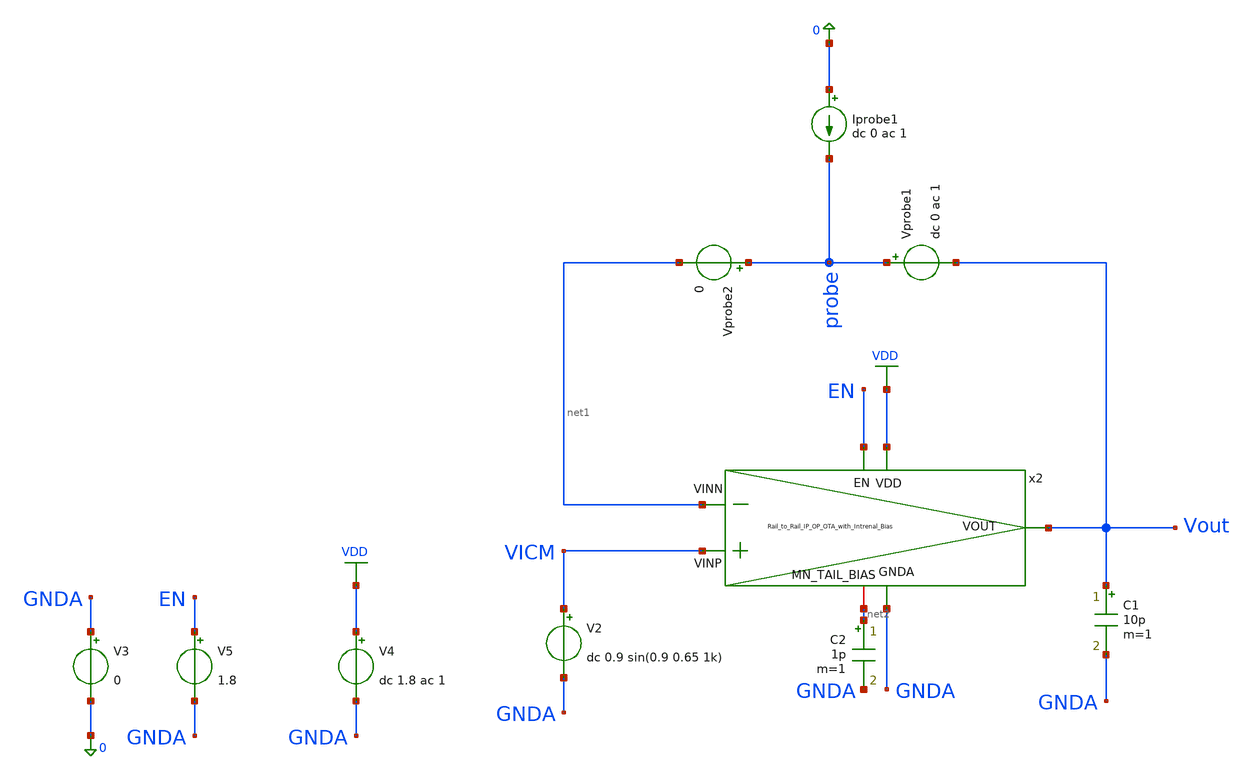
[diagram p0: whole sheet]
** sch_path: OTAs/Rail_to_Rail_OTA_Inp_IP/With_internal_Bias/tb_Rail_to_Rail_IP_OP_OTA_int_bias_STB.sch
.lib $::SKYWATER_MODELS/sky130.lib.spice tt
.include $::SKYWATER_STDCELLS/sky130_fd_sc_hd.spice

**.subckt tb_Rail_to_Rail_IP_OP_OTA_int_bias_STB
V3 GNDA 0 0
V5 EN GNDA 1.8
C1 Vout GNDA 10p m=1
Vprobe1 probe Vout dc 0 ac 1
Vprobe2 probe net1 0
Iprobe1 0 probe dc 0 ac 1
V2 VICM GNDA dc 0.9 sin(0.9 0.65 1k)
V4 VDD GNDA dc 1.8 ac 1
C2 net2 GNDA 1p m=1
x2 VDD EN net1 Vout VICM net2 GNDA Rail_to_Rail_IP_OP_OTA_with_Intrenal_Bias
**** begin user architecture code



.save @m.x1.xmn_bot_l2.msky130_fd_pr__nfet_01v8[gm]
.save @m.x1.xmn_bot_l2.msky130_fd_pr__nfet_01v8[gds]
.save @m.x1.xmn_bot_l2.msky130_fd_pr__nfet_01v8[vth]
.save @m.x1.xmn_bot_l2.msky130_fd_pr__nfet_01v8[vdsat]
.save @m.x1.xmn_bot_l2.msky130_fd_pr__nfet_01v8[cgg]
.save @m.x1.xmn_bot_l2.msky130_fd_pr__nfet_01v8[cgso]
.save @m.x1.xmn_bot_l2.msky130_fd_pr__nfet_01v8[cgdo]
.save @m.x1.xmn_casc_l2.msky130_fd_pr__nfet_01v8[gm]
.save @m.x1.xmn_casc_l2.msky130_fd_pr__nfet_01v8[gds]
.save @m.x1.xmn_casc_l2.msky130_fd_pr__nfet_01v8[vth]
.save @m.x1.xmn_casc_l2.msky130_fd_pr__nfet_01v8[vdsat]
.save @m.x1.xmn_casc_l2.msky130_fd_pr__nfet_01v8[cgg]
.save @m.x1.xmn_casc_l2.msky130_fd_pr__nfet_01v8[cgso]
.save @m.x1.xmn_casc_l2.msky130_fd_pr__nfet_01v8[cgdo]
.save @m.x1.xmn_bot_l1.msky130_fd_pr__nfet_01v8[gm]
.save @m.x1.xmn_bot_l1.msky130_fd_pr__nfet_01v8[gds]
.save @m.x1.xmn_bot_l1.msky130_fd_pr__nfet_01v8[vth]
.save @m.x1.xmn_bot_l1.msky130_fd_pr__nfet_01v8[vdsat]
.save @m.x1.xmn_bot_l1.msky130_fd_pr__nfet_01v8[cgg]
.save @m.x1.xmn_bot_l1.msky130_fd_pr__nfet_01v8[cgso]
.save @m.x1.xmn_bot_l1.msky130_fd_pr__nfet_01v8[cgdo]
.save @m.x1.xmn_casc_l1.msky130_fd_pr__nfet_01v8[gm]
.save @m.x1.xmn_casc_l1.msky130_fd_pr__nfet_01v8[gds]
.save @m.x1.xmn_casc_l1.msky130_fd_pr__nfet_01v8[vth]
.save @m.x1.xmn_casc_l1.msky130_fd_pr__nfet_01v8[vdsat]
.save @m.x1.xmn_casc_l1.msky130_fd_pr__nfet_01v8[cgg]
.save @m.x1.xmn_casc_l1.msky130_fd_pr__nfet_01v8[cgso]
.save @m.x1.xmn_casc_l1.msky130_fd_pr__nfet_01v8[cgdo]
.save @m.x1.xmp_casc_l2.msky130_fd_pr__pfet_01v8[gm]
.save @m.x1.xmp_casc_l2.msky130_fd_pr__pfet_01v8[gds]
.save @m.x1.xmp_casc_l2.msky130_fd_pr__pfet_01v8[vth]
.save @m.x1.xmp_casc_l2.msky130_fd_pr__pfet_01v8[vdsat]
.save @m.x1.xmp_casc_l2.msky130_fd_pr__pfet_01v8[cgg]
.save @m.x1.xmp_casc_l2.msky130_fd_pr__pfet_01v8[cgso]
.save @m.x1.xmp_casc_l2.msky130_fd_pr__pfet_01v8[cgdo]
.save @m.x1.xmp_casc_l1.msky130_fd_pr__pfet_01v8[gm]
.save @m.x1.xmp_casc_l1.msky130_fd_pr__pfet_01v8[gds]
.save @m.x1.xmp_casc_l1.msky130_fd_pr__pfet_01v8[vth]
.save @m.x1.xmp_casc_l1.msky130_fd_pr__pfet_01v8[vdsat]
.save @m.x1.xmp_casc_l1.msky130_fd_pr__pfet_01v8[cgg]
.save @m.x1.xmp_casc_l1.msky130_fd_pr__pfet_01v8[cgso]
.save @m.x1.xmp_casc_l1.msky130_fd_pr__pfet_01v8[cgdo]
.save @m.x1.xmp_top_l1.msky130_fd_pr__pfet_01v8[gm]
.save @m.x1.xmp_top_l1.msky130_fd_pr__pfet_01v8[gds]
.save @m.x1.xmp_top_l1.msky130_fd_pr__pfet_01v8[vth]
.save @m.x1.xmp_top_l1.msky130_fd_pr__pfet_01v8[vdsat]
.save @m.x1.xmp_top_l1.msky130_fd_pr__pfet_01v8[cgg]
.save @m.x1.xmp_top_l1.msky130_fd_pr__pfet_01v8[cgso]
.save @m.x1.xmp_top_l1.msky130_fd_pr__pfet_01v8[cgdo]
.save @m.x1.xmn_a1.msky130_fd_pr__nfet_01v8_lvt[gm]
.save @m.x1.xmn_a1.msky130_fd_pr__nfet_01v8_lvt[gds]
.save @m.x1.xmn_a1.msky130_fd_pr__nfet_01v8_lvt[vth]
.save @m.x1.xmn_a1.msky130_fd_pr__nfet_01v8_lvt[vdsat]
.save @m.x1.xmn_a1.msky130_fd_pr__nfet_01v8_lvt[cgg]
.save @m.x1.xmn_a1.msky130_fd_pr__nfet_01v8_lvt[cgso]
.save @m.x1.xmn_a1.msky130_fd_pr__nfet_01v8_lvt[cgdo]
.save @m.x1.xmn_a2.msky130_fd_pr__nfet_01v8_lvt[gm]
.save @m.x1.xmn_a2.msky130_fd_pr__nfet_01v8_lvt[gds]
.save @m.x1.xmn_a2.msky130_fd_pr__nfet_01v8_lvt[vth]
.save @m.x1.xmn_a2.msky130_fd_pr__nfet_01v8_lvt[vdsat]
.save @m.x1.xmn_a2.msky130_fd_pr__nfet_01v8_lvt[cgg]
.save @m.x1.xmn_a2.msky130_fd_pr__nfet_01v8_lvt[cgso]
.save @m.x1.xmn_a2.msky130_fd_pr__nfet_01v8_lvt[cgdo]
.save @m.x1.xmp_a1.msky130_fd_pr__pfet_01v8_lvt[gm]
.save @m.x1.xmp_a1.msky130_fd_pr__pfet_01v8_lvt[gds]
.save @m.x1.xmp_a1.msky130_fd_pr__pfet_01v8_lvt[vth]
.save @m.x1.xmp_a1.msky130_fd_pr__pfet_01v8_lvt[vdsat]
.save @m.x1.xmp_a1.msky130_fd_pr__pfet_01v8_lvt[cgg]
.save @m.x1.xmp_a1.msky130_fd_pr__pfet_01v8_lvt[cgso]
.save @m.x1.xmp_a1.msky130_fd_pr__pfet_01v8_lvt[cgdo]
.save @m.x1.xmp_a2.msky130_fd_pr__pfet_01v8_lvt[gm]
.save @m.x1.xmp_a2.msky130_fd_pr__pfet_01v8_lvt[gds]
.save @m.x1.xmp_a2.msky130_fd_pr__pfet_01v8_lvt[vth]
.save @m.x1.xmp_a2.msky130_fd_pr__pfet_01v8_lvt[vdsat]
.save @m.x1.xmp_a2.msky130_fd_pr__pfet_01v8_lvt[cgg]
.save @m.x1.xmp_a2.msky130_fd_pr__pfet_01v8_lvt[cgso]
.save @m.x1.xmp_a2.msky130_fd_pr__pfet_01v8_lvt[cgdo]
.save @m.x1.xmp_pdiff_bias.msky130_fd_pr__pfet_01v8[gm]
.save @m.x1.xmp_pdiff_bias.msky130_fd_pr__pfet_01v8[gds]
.save @m.x1.xmp_pdiff_bias.msky130_fd_pr__pfet_01v8[vth]
.save @m.x1.xmp_pdiff_bias.msky130_fd_pr__pfet_01v8[vdsat]
.save @m.x1.xmp_pdiff_bias.msky130_fd_pr__pfet_01v8[cgg]
.save @m.x1.xmp_pdiff_bias.msky130_fd_pr__pfet_01v8[cgso]
.save @m.x1.xmp_pdiff_bias.msky130_fd_pr__pfet_01v8[cgdo]
.save @m.x1.xmn_ndiff_bias.msky130_fd_pr__nfet_01v8[gm]
.save @m.x1.xmn_ndiff_bias.msky130_fd_pr__nfet_01v8[gds]
.save @m.x1.xmn_ndiff_bias.msky130_fd_pr__nfet_01v8[vth]
.save @m.x1.xmn_ndiff_bias.msky130_fd_pr__nfet_01v8[vdsat]
.save @m.x1.xmn_ndiff_bias.msky130_fd_pr__nfet_01v8[cgg]
.save @m.x1.xmn_ndiff_bias.msky130_fd_pr__nfet_01v8[cgso]
.save @m.x1.xmn_ndiff_bias.msky130_fd_pr__nfet_01v8[cgdo]
.save @m.x1.xmp_pdiff_bias_b.msky130_fd_pr__pfet_01v8[gm]
.save @m.x1.xmp_pdiff_bias_b.msky130_fd_pr__pfet_01v8[gds]
.save @m.x1.xmp_pdiff_bias_b.msky130_fd_pr__pfet_01v8[vth]
.save @m.x1.xmp_pdiff_bias_b.msky130_fd_pr__pfet_01v8[vdsat]
.save @m.x1.xmp_pdiff_bias_b.msky130_fd_pr__pfet_01v8[cgg]
.save @m.x1.xmp_pdiff_bias_b.msky130_fd_pr__pfet_01v8[cgso]
.save @m.x1.xmp_pdiff_bias_b.msky130_fd_pr__pfet_01v8[cgdo]
.save @m.x1.xmp_top_l2.msky130_fd_pr__pfet_01v8[gm]
.save @m.x1.xmp_top_l2.msky130_fd_pr__pfet_01v8[gds]
.save @m.x1.xmp_top_l2.msky130_fd_pr__pfet_01v8[vth]
.save @m.x1.xmp_top_l2.msky130_fd_pr__pfet_01v8[vdsat]
.save @m.x1.xmp_top_l2.msky130_fd_pr__pfet_01v8[cgg]
.save @m.x1.xmp_top_l2.msky130_fd_pr__pfet_01v8[cgso]
.save @m.x1.xmp_top_l2.msky130_fd_pr__pfet_01v8[cgdo]
.save @m.x1.xmn_bias_source.msky130_fd_pr__nfet_01v8[gm]
.save @m.x1.xmn_bias_source.msky130_fd_pr__nfet_01v8[gds]
.save @m.x1.xmn_bias_source.msky130_fd_pr__nfet_01v8[vth]
.save @m.x1.xmn_bias_source.msky130_fd_pr__nfet_01v8[vdsat]
.save @m.x1.xmn_bias_source.msky130_fd_pr__nfet_01v8[cgg]
.save @m.x1.xmn_bias_source.msky130_fd_pr__nfet_01v8[cgso]
.save @m.x1.xmn_bias_source.msky130_fd_pr__nfet_01v8[cgdo]
.save @m.x1.xmn_bias_ext.msky130_fd_pr__nfet_01v8[gm]
.save @m.x1.xmn_bias_ext.msky130_fd_pr__nfet_01v8[gds]
.save @m.x1.xmn_bias_ext.msky130_fd_pr__nfet_01v8[vth]
.save @m.x1.xmn_bias_ext.msky130_fd_pr__nfet_01v8[vdsat]
.save @m.x1.xmn_bias_ext.msky130_fd_pr__nfet_01v8[cgg]
.save @m.x1.xmn_bias_ext.msky130_fd_pr__nfet_01v8[cgso]
.save @m.x1.xmn_bias_ext.msky130_fd_pr__nfet_01v8[cgdo]
.save @m.x1.xmp_casc_b_source.msky130_fd_pr__pfet_01v8[gm]
.save @m.x1.xmp_casc_b_source.msky130_fd_pr__pfet_01v8[gds]
.save @m.x1.xmp_casc_b_source.msky130_fd_pr__pfet_01v8[vth]
.save @m.x1.xmp_casc_b_source.msky130_fd_pr__pfet_01v8[vdsat]
.save @m.x1.xmp_casc_b_source.msky130_fd_pr__pfet_01v8[cgg]
.save @m.x1.xmp_casc_b_source.msky130_fd_pr__pfet_01v8[cgso]
.save @m.x1.xmp_casc_b_source.msky130_fd_pr__pfet_01v8[cgdo]
.save @m.x1.xmn_casc_bias8.msky130_fd_pr__nfet_01v8[gm]
.save @m.x1.xmn_casc_bias8.msky130_fd_pr__nfet_01v8[gds]
.save @m.x1.xmn_casc_bias8.msky130_fd_pr__nfet_01v8[vth]
.save @m.x1.xmn_casc_bias8.msky130_fd_pr__nfet_01v8[vdsat]
.save @m.x1.xmn_casc_bias8.msky130_fd_pr__nfet_01v8[cgg]
.save @m.x1.xmn_casc_bias8.msky130_fd_pr__nfet_01v8[cgso]
.save @m.x1.xmn_casc_bias8.msky130_fd_pr__nfet_01v8[cgdo]
.save @m.x1.xmn_casc_b_source.msky130_fd_pr__nfet_01v8[gm]
.save @m.x1.xmn_casc_b_source.msky130_fd_pr__nfet_01v8[gds]
.save @m.x1.xmn_casc_b_source.msky130_fd_pr__nfet_01v8[vth]
.save @m.x1.xmn_casc_b_source.msky130_fd_pr__nfet_01v8[vdsat]
.save @m.x1.xmn_casc_b_source.msky130_fd_pr__nfet_01v8[cgg]
.save @m.x1.xmn_casc_b_source.msky130_fd_pr__nfet_01v8[cgso]
.save @m.x1.xmn_casc_b_source.msky130_fd_pr__nfet_01v8[cgdo]
.save @m.x1.xmp_casc_bias1.msky130_fd_pr__pfet_01v8[gm]
.save @m.x1.xmp_casc_bias1.msky130_fd_pr__pfet_01v8[gds]
.save @m.x1.xmp_casc_bias1.msky130_fd_pr__pfet_01v8[vth]
.save @m.x1.xmp_casc_bias1.msky130_fd_pr__pfet_01v8[vdsat]
.save @m.x1.xmp_casc_bias1.msky130_fd_pr__pfet_01v8[cgg]
.save @m.x1.xmp_casc_bias1.msky130_fd_pr__pfet_01v8[cgso]
.save @m.x1.xmp_casc_bias1.msky130_fd_pr__pfet_01v8[cgdo]
.save @m.x1.xmn_casc_bias7.msky130_fd_pr__nfet_01v8[gm]
.save @m.x1.xmn_casc_bias7.msky130_fd_pr__nfet_01v8[gds]
.save @m.x1.xmn_casc_bias7.msky130_fd_pr__nfet_01v8[vth]
.save @m.x1.xmn_casc_bias7.msky130_fd_pr__nfet_01v8[vdsat]
.save @m.x1.xmn_casc_bias7.msky130_fd_pr__nfet_01v8[cgg]
.save @m.x1.xmn_casc_bias7.msky130_fd_pr__nfet_01v8[cgso]
.save @m.x1.xmn_casc_bias7.msky130_fd_pr__nfet_01v8[cgdo]
.save @m.x1.xmn_casc_bias6.msky130_fd_pr__nfet_01v8[gm]
.save @m.x1.xmn_casc_bias6.msky130_fd_pr__nfet_01v8[gds]
.save @m.x1.xmn_casc_bias6.msky130_fd_pr__nfet_01v8[vth]
.save @m.x1.xmn_casc_bias6.msky130_fd_pr__nfet_01v8[vdsat]
.save @m.x1.xmn_casc_bias6.msky130_fd_pr__nfet_01v8[cgg]
.save @m.x1.xmn_casc_bias6.msky130_fd_pr__nfet_01v8[cgso]
.save @m.x1.xmn_casc_bias6.msky130_fd_pr__nfet_01v8[cgdo]
.save @m.x1.xmp_casc_bias2.msky130_fd_pr__pfet_01v8[gm]
.save @m.x1.xmp_casc_bias2.msky130_fd_pr__pfet_01v8[gds]
.save @m.x1.xmp_casc_bias2.msky130_fd_pr__pfet_01v8[vth]
.save @m.x1.xmp_casc_bias2.msky130_fd_pr__pfet_01v8[vdsat]
.save @m.x1.xmp_casc_bias2.msky130_fd_pr__pfet_01v8[cgg]
.save @m.x1.xmp_casc_bias2.msky130_fd_pr__pfet_01v8[cgso]
.save @m.x1.xmp_casc_bias2.msky130_fd_pr__pfet_01v8[cgdo]
.save @m.x1.xmp_casc_bias3.msky130_fd_pr__pfet_01v8[gm]
.save @m.x1.xmp_casc_bias3.msky130_fd_pr__pfet_01v8[gds]
.save @m.x1.xmp_casc_bias3.msky130_fd_pr__pfet_01v8[vth]
.save @m.x1.xmp_casc_bias3.msky130_fd_pr__pfet_01v8[vdsat]
.save @m.x1.xmp_casc_bias3.msky130_fd_pr__pfet_01v8[cgg]
.save @m.x1.xmp_casc_bias3.msky130_fd_pr__pfet_01v8[cgso]
.save @m.x1.xmp_casc_bias3.msky130_fd_pr__pfet_01v8[cgdo]
.save @m.x1.xmn_casc_bias5.msky130_fd_pr__nfet_01v8[gm]
.save @m.x1.xmn_casc_bias5.msky130_fd_pr__nfet_01v8[gds]
.save @m.x1.xmn_casc_bias5.msky130_fd_pr__nfet_01v8[vth]
.save @m.x1.xmn_casc_bias5.msky130_fd_pr__nfet_01v8[vdsat]
.save @m.x1.xmn_casc_bias5.msky130_fd_pr__nfet_01v8[cgg]
.save @m.x1.xmn_casc_bias5.msky130_fd_pr__nfet_01v8[cgso]
.save @m.x1.xmn_casc_bias5.msky130_fd_pr__nfet_01v8[cgdo]
.save @m.x1.xmn_casc_bias4.msky130_fd_pr__nfet_01v8[gm]
.save @m.x1.xmn_casc_bias4.msky130_fd_pr__nfet_01v8[gds]
.save @m.x1.xmn_casc_bias4.msky130_fd_pr__nfet_01v8[vth]
.save @m.x1.xmn_casc_bias4.msky130_fd_pr__nfet_01v8[vdsat]
.save @m.x1.xmn_casc_bias4.msky130_fd_pr__nfet_01v8[cgg]
.save @m.x1.xmn_casc_bias4.msky130_fd_pr__nfet_01v8[cgso]
.save @m.x1.xmn_casc_bias4.msky130_fd_pr__nfet_01v8[cgdo]
.save @m.x1.xmn_casc_bias3.msky130_fd_pr__nfet_01v8[gm]
.save @m.x1.xmn_casc_bias3.msky130_fd_pr__nfet_01v8[gds]
.save @m.x1.xmn_casc_bias3.msky130_fd_pr__nfet_01v8[vth]
.save @m.x1.xmn_casc_bias3.msky130_fd_pr__nfet_01v8[vdsat]
.save @m.x1.xmn_casc_bias3.msky130_fd_pr__nfet_01v8[cgg]
.save @m.x1.xmn_casc_bias3.msky130_fd_pr__nfet_01v8[cgso]
.save @m.x1.xmn_casc_bias3.msky130_fd_pr__nfet_01v8[cgdo]
.save @m.x1.xmn_casc_bias1.msky130_fd_pr__nfet_01v8[gm]
.save @m.x1.xmn_casc_bias1.msky130_fd_pr__nfet_01v8[gds]
.save @m.x1.xmn_casc_bias1.msky130_fd_pr__nfet_01v8[vth]
.save @m.x1.xmn_casc_bias1.msky130_fd_pr__nfet_01v8[vdsat]
.save @m.x1.xmn_casc_bias1.msky130_fd_pr__nfet_01v8[cgg]
.save @m.x1.xmn_casc_bias1.msky130_fd_pr__nfet_01v8[cgso]
.save @m.x1.xmn_casc_bias1.msky130_fd_pr__nfet_01v8[cgdo]
.save @m.x1.xmn_casc_bias2.msky130_fd_pr__nfet_01v8[gm]
.save @m.x1.xmn_casc_bias2.msky130_fd_pr__nfet_01v8[gds]
.save @m.x1.xmn_casc_bias2.msky130_fd_pr__nfet_01v8[vth]
.save @m.x1.xmn_casc_bias2.msky130_fd_pr__nfet_01v8[vdsat]
.save @m.x1.xmn_casc_bias2.msky130_fd_pr__nfet_01v8[cgg]
.save @m.x1.xmn_casc_bias2.msky130_fd_pr__nfet_01v8[cgso]
.save @m.x1.xmn_casc_bias2.msky130_fd_pr__nfet_01v8[cgdo]
.save @m.x1.xmn_sw1.msky130_fd_pr__nfet_01v8[gm]
.save @m.x1.xmn_sw1.msky130_fd_pr__nfet_01v8[gds]
.save @m.x1.xmn_sw1.msky130_fd_pr__nfet_01v8[vth]
.save @m.x1.xmn_sw1.msky130_fd_pr__nfet_01v8[vdsat]
.save @m.x1.xmn_sw1.msky130_fd_pr__nfet_01v8[cgg]
.save @m.x1.xmn_sw1.msky130_fd_pr__nfet_01v8[cgso]
.save @m.x1.xmn_sw1.msky130_fd_pr__nfet_01v8[cgdo]
.save @m.x1.xmp_sw1.msky130_fd_pr__pfet_01v8[gm]
.save @m.x1.xmp_sw1.msky130_fd_pr__pfet_01v8[gds]
.save @m.x1.xmp_sw1.msky130_fd_pr__pfet_01v8[vth]
.save @m.x1.xmp_sw1.msky130_fd_pr__pfet_01v8[vdsat]
.save @m.x1.xmp_sw1.msky130_fd_pr__pfet_01v8[cgg]
.save @m.x1.xmp_sw1.msky130_fd_pr__pfet_01v8[cgso]
.save @m.x1.xmp_sw1.msky130_fd_pr__pfet_01v8[cgdo]
.save @m.x1.xmp_sw2.msky130_fd_pr__pfet_01v8[gm]
.save @m.x1.xmp_sw2.msky130_fd_pr__pfet_01v8[gds]
.save @m.x1.xmp_sw2.msky130_fd_pr__pfet_01v8[vth]
.save @m.x1.xmp_sw2.msky130_fd_pr__pfet_01v8[vdsat]
.save @m.x1.xmp_sw2.msky130_fd_pr__pfet_01v8[cgg]
.save @m.x1.xmp_sw2.msky130_fd_pr__pfet_01v8[cgso]
.save @m.x1.xmp_sw2.msky130_fd_pr__pfet_01v8[cgdo]
.save @m.x1.xmn_sw2.msky130_fd_pr__nfet_01v8[gm]
.save @m.x1.xmn_sw2.msky130_fd_pr__nfet_01v8[gds]
.save @m.x1.xmn_sw2.msky130_fd_pr__nfet_01v8[vth]
.save @m.x1.xmn_sw2.msky130_fd_pr__nfet_01v8[vdsat]
.save @m.x1.xmn_sw2.msky130_fd_pr__nfet_01v8[cgg]
.save @m.x1.xmn_sw2.msky130_fd_pr__nfet_01v8[cgso]
.save @m.x1.xmn_sw2.msky130_fd_pr__nfet_01v8[cgdo]
.save @m.x1.xmp_sw3.msky130_fd_pr__pfet_01v8[gm]
.save @m.x1.xmp_sw3.msky130_fd_pr__pfet_01v8[gds]
.save @m.x1.xmp_sw3.msky130_fd_pr__pfet_01v8[vth]
.save @m.x1.xmp_sw3.msky130_fd_pr__pfet_01v8[vdsat]
.save @m.x1.xmp_sw3.msky130_fd_pr__pfet_01v8[cgg]
.save @m.x1.xmp_sw3.msky130_fd_pr__pfet_01v8[cgso]
.save @m.x1.xmp_sw3.msky130_fd_pr__pfet_01v8[cgdo]




.options savecurrents
.control
 save all
 let runs=2
 let run=0

 alter @Vprobe1[acmag]=1
 alter @iprobe1[acmag]=0

 dowhile run < runs
 set run =”$&run”
 ac dec 20 1 1e8
 write OTA_STB_TB_{$run}.raw
 all
 alter @Vprobe1[acmag]=0
 alter @iprobe1[acmag]=1
 let run = run + 1
 end

 let ip22 = ac2.i(Vprobe2)
 let vprb1 = ac1.probe
 let mb = 1/(vprb1+ip22)-1
 let phase_mb = 180/PI*vp(mb)
 plot vdb(mb)
 plot phase_mb
 plot vdb(mb) phase_mb
 echo -------------------------------
 echo -------------------------------
 meas ac peak MAX vmag(mb) FROM=2 TO=1.5GHZ
 let f3db = peak/sqrt(2)
 meas ac f1 WHEN vmag(mb)=f3db RISE=1
 meas ac BW WHEN vmag(mb)=f3db FALL=1
 let GBW = peak*BW
 meas ac pm_deg find phase_mb when vdb(mb)=0
 meas ac dominant_pole_f when vdb(mb)=0
 meas ac loop_gain find vdb(mb) at=0.01
 print GBW
 op
 **show m : gm : gmbs : gds : vds : vdsat : vgs : vth : id
.endc

**** end user architecture code
**.ends

* expanding   symbol:
*+  /home/nithin/eda/SKY130_DESIGN_IPS/OTAs/Rail_to_Rail_OTA_Inp_IP/Single_ended/With_internal_Bias/Rail_to_Rail_IP_OP_OTA_with_Intrenal_Bias.sym # of pins=7
** sym_path: OTAs/Rail_to_Rail_OTA_Inp_IP/With_internal_Bias/SCH/Rail_to_Rail_IP_OP_OTA_with_Intrenal_Bias.sym
** sch_path: OTAs/Rail_to_Rail_OTA_Inp_IP/With_internal_Bias/SCH/Rail_to_Rail_IP_OP_OTA_with_Intrenal_Bias.sch
.subckt Rail_to_Rail_IP_OP_OTA_with_Intrenal_Bias VDD EN VINN VOUT VINP MN_TAIL_BIAS GNDA
*.ipin VINP
*.ipin VINN
*.ipin VDD
*.ipin GNDA
*.opin VOUT
*.ipin EN
*.iopin MN_TAIL_BIAS
XMN_BOT_L2 net2 net8 GNDA GND sky130_fd_pr__nfet_01v8 L=2 W=0.5 nf=1 ad='int((1 + 1)/2) * 0.5 / 1 * 0.29'
+ as='int((1 + 2)/2) * 0.5 / 1 * 0.29' pd='2*int((1 + 1)/2) * (0.5 / 1 + 0.29)' ps='2*int((1 + 2)/2) * (0.5 / 1 + 0.29)'
+ nrd='0.29 / 0.5 ' nrs='0.29 / 0.5 ' sa=0 sb=0 sd=0 mult=6 m=6
XMN_CASC_L2 VOUT VBN_CASC net2 GND sky130_fd_pr__nfet_01v8 L=0.5 W=0.5 nf=1 ad='int((1 + 1)/2) * 0.5 / 1 * 0.29'
+ as='int((1 + 2)/2) * 0.5 / 1 * 0.29' pd='2*int((1 + 1)/2) * (0.5 / 1 + 0.29)' ps='2*int((1 + 2)/2) * (0.5 / 1 + 0.29)'
+ nrd='0.29 / 0.5 ' nrs='0.29 / 0.5 ' sa=0 sb=0 sd=0 mult=3 m=3
XMN_BOT_L1 net1 net8 GNDA GND sky130_fd_pr__nfet_01v8 L=2 W=0.5 nf=1 ad='int((1 + 1)/2) * 0.5 / 1 * 0.29'
+ as='int((1 + 2)/2) * 0.5 / 1 * 0.29' pd='2*int((1 + 1)/2) * (0.5 / 1 + 0.29)' ps='2*int((1 + 2)/2) * (0.5 / 1 + 0.29)'
+ nrd='0.29 / 0.5 ' nrs='0.29 / 0.5 ' sa=0 sb=0 sd=0 mult=6 m=6
XMN_CASC_L1 net5 VBN_CASC net1 GND sky130_fd_pr__nfet_01v8 L=0.5 W=0.5 nf=1 ad='int((1 + 1)/2) * 0.5 / 1 * 0.29'
+ as='int((1 + 2)/2) * 0.5 / 1 * 0.29' pd='2*int((1 + 1)/2) * (0.5 / 1 + 0.29)' ps='2*int((1 + 2)/2) * (0.5 / 1 + 0.29)'
+ nrd='0.29 / 0.5 ' nrs='0.29 / 0.5 ' sa=0 sb=0 sd=0 mult=3 m=3
XMP_CASC_L2 VOUT VBP_CASC net4 VDD sky130_fd_pr__pfet_01v8 L=0.5 W=0.5 nf=1 ad='int((1 + 1)/2) * 0.5 / 1 * 0.29'
+ as='int((1 + 2)/2) * 0.5 / 1 * 0.29' pd='2*int((1 + 1)/2) * (0.5 / 1 + 0.29)' ps='2*int((1 + 2)/2) * (0.5 / 1 + 0.29)'
+ nrd='0.29 / 0.5 ' nrs='0.29 / 0.5 ' sa=0 sb=0 sd=0 mult=8 m=8
XMP_CASC_L1 net5 VBP_CASC net3 VDD sky130_fd_pr__pfet_01v8 L=0.5 W=0.5 nf=1 ad='int((1 + 1)/2) * 0.5 / 1 * 0.29'
+ as='int((1 + 2)/2) * 0.5 / 1 * 0.29' pd='2*int((1 + 1)/2) * (0.5 / 1 + 0.29)' ps='2*int((1 + 2)/2) * (0.5 / 1 + 0.29)'
+ nrd='0.29 / 0.5 ' nrs='0.29 / 0.5 ' sa=0 sb=0 sd=0 mult=8 m=8
XMP_TOP_L1 net3 net5 VDD VDD sky130_fd_pr__pfet_01v8 L=2 W=2 nf=1 ad='int((1 + 1)/2) * 2 / 1 * 0.29'
+ as='int((1 + 2)/2) * 2 / 1 * 0.29' pd='2*int((1 + 1)/2) * (2 / 1 + 0.29)' ps='2*int((1 + 2)/2) * (2 / 1 + 0.29)'
+ nrd='0.29 / 2 ' nrs='0.29 / 2 ' sa=0 sb=0 sd=0 mult=6 m=6
XMN_A1 net3 VINP net6 GND sky130_fd_pr__nfet_01v8_lvt L=2 W=2.5 nf=1 ad='int((1 + 1)/2) * 2.5 / 1 * 0.29'
+ as='int((1 + 2)/2) * 2.5 / 1 * 0.29' pd='2*int((1 + 1)/2) * (2.5 / 1 + 0.29)' ps='2*int((1 + 2)/2) * (2.5 / 1 + 0.29)'
+ nrd='0.29 / 2.5 ' nrs='0.29 / 2.5 ' sa=0 sb=0 sd=0 mult=8 m=8
XMN_A2 net4 VINN net6 GND sky130_fd_pr__nfet_01v8_lvt L=2 W=2.5 nf=1 ad='int((1 + 1)/2) * 2.5 / 1 * 0.29'
+ as='int((1 + 2)/2) * 2.5 / 1 * 0.29' pd='2*int((1 + 1)/2) * (2.5 / 1 + 0.29)' ps='2*int((1 + 2)/2) * (2.5 / 1 + 0.29)'
+ nrd='0.29 / 2.5 ' nrs='0.29 / 2.5 ' sa=0 sb=0 sd=0 mult=8 m=8
XMP_A1 net1 VINP net7 VDD sky130_fd_pr__pfet_01v8_lvt L=2 W=4 nf=1 ad='int((1 + 1)/2) * 4 / 1 * 0.29'
+ as='int((1 + 2)/2) * 4 / 1 * 0.29' pd='2*int((1 + 1)/2) * (4 / 1 + 0.29)' ps='2*int((1 + 2)/2) * (4 / 1 + 0.29)'
+ nrd='0.29 / 4 ' nrs='0.29 / 4 ' sa=0 sb=0 sd=0 mult=28 m=28
XMP_A2 net2 VINN net7 VDD sky130_fd_pr__pfet_01v8_lvt L=2 W=4 nf=1 ad='int((1 + 1)/2) * 4 / 1 * 0.29'
+ as='int((1 + 2)/2) * 4 / 1 * 0.29' pd='2*int((1 + 1)/2) * (4 / 1 + 0.29)' ps='2*int((1 + 2)/2) * (4 / 1 + 0.29)'
+ nrd='0.29 / 4 ' nrs='0.29 / 4 ' sa=0 sb=0 sd=0 mult=28 m=28
XMP_PDIFF_BIAS net7 net9 VDD VDD sky130_fd_pr__pfet_01v8 L=2 W=2 nf=1 ad='int((1 + 1)/2) * 2 / 1 * 0.29'
+ as='int((1 + 2)/2) * 2 / 1 * 0.29' pd='2*int((1 + 1)/2) * (2 / 1 + 0.29)' ps='2*int((1 + 2)/2) * (2 / 1 + 0.29)'
+ nrd='0.29 / 2 ' nrs='0.29 / 2 ' sa=0 sb=0 sd=0 mult=8 m=8
XMN_NDIFF_BIAS net6 net8 GNDA GND sky130_fd_pr__nfet_01v8 L=2 W=0.5 nf=1 ad='int((1 + 1)/2) * 0.5 / 1 * 0.29'
+ as='int((1 + 2)/2) * 0.5 / 1 * 0.29' pd='2*int((1 + 1)/2) * (0.5 / 1 + 0.29)' ps='2*int((1 + 2)/2) * (0.5 / 1 + 0.29)'
+ nrd='0.29 / 0.5 ' nrs='0.29 / 0.5 ' sa=0 sb=0 sd=0 mult=8 m=8
XMP_PDIFF_BIAS_B net9 net9 VDD VDD sky130_fd_pr__pfet_01v8 L=2 W=2 nf=1 ad='int((1 + 1)/2) * 2 / 1 * 0.29'
+ as='int((1 + 2)/2) * 2 / 1 * 0.29' pd='2*int((1 + 1)/2) * (2 / 1 + 0.29)' ps='2*int((1 + 2)/2) * (2 / 1 + 0.29)'
+ nrd='0.29 / 2 ' nrs='0.29 / 2 ' sa=0 sb=0 sd=0 mult=1 m=1
XMP_TOP_L2 net4 net5 VDD VDD sky130_fd_pr__pfet_01v8 L=2 W=2 nf=1 ad='int((1 + 1)/2) * 2 / 1 * 0.29'
+ as='int((1 + 2)/2) * 2 / 1 * 0.29' pd='2*int((1 + 1)/2) * (2 / 1 + 0.29)' ps='2*int((1 + 2)/2) * (2 / 1 + 0.29)'
+ nrd='0.29 / 2 ' nrs='0.29 / 2 ' sa=0 sb=0 sd=0 mult=6 m=6
XMN_BIAS_SOURCE net9 net8 GNDA GND sky130_fd_pr__nfet_01v8 L=2 W=0.5 nf=1 ad='int((1 + 1)/2) * 0.5 / 1 * 0.29'
+ as='int((1 + 2)/2) * 0.5 / 1 * 0.29' pd='2*int((1 + 1)/2) * (0.5 / 1 + 0.29)' ps='2*int((1 + 2)/2) * (0.5 / 1 + 0.29)'
+ nrd='0.29 / 0.5 ' nrs='0.29 / 0.5 ' sa=0 sb=0 sd=0 mult=1 m=1
XMN_BIAS_EXT net8 net8 GNDA GND sky130_fd_pr__nfet_01v8 L=2 W=0.5 nf=1 ad='int((1 + 1)/2) * 0.5 / 1 * 0.29'
+ as='int((1 + 2)/2) * 0.5 / 1 * 0.29' pd='2*int((1 + 1)/2) * (0.5 / 1 + 0.29)' ps='2*int((1 + 2)/2) * (0.5 / 1 + 0.29)'
+ nrd='0.29 / 0.5 ' nrs='0.29 / 0.5 ' sa=0 sb=0 sd=0 mult=1 m=1
XMP_CASC_B_SOURCE VBN_CASC net9 VDD VDD sky130_fd_pr__pfet_01v8 L=2 W=2 nf=1 ad='int((1 + 1)/2) * 2 / 1 * 0.29'
+ as='int((1 + 2)/2) * 2 / 1 * 0.29' pd='2*int((1 + 1)/2) * (2 / 1 + 0.29)' ps='2*int((1 + 2)/2) * (2 / 1 + 0.29)'
+ nrd='0.29 / 2 ' nrs='0.29 / 2 ' sa=0 sb=0 sd=0 mult=1 m=1
XMN_CASC_BIAS8 net16 VBN_CASC GNDA GND sky130_fd_pr__nfet_01v8 L=0.5 W=0.5 nf=1 ad='int((1 + 1)/2) * 0.5 / 1 * 0.29'
+ as='int((1 + 2)/2) * 0.5 / 1 * 0.29' pd='2*int((1 + 1)/2) * (0.5 / 1 + 0.29)' ps='2*int((1 + 2)/2) * (0.5 / 1 + 0.29)'
+ nrd='0.29 / 0.5 ' nrs='0.29 / 0.5 ' sa=0 sb=0 sd=0 mult=1 m=1
XMN_CASC_B_SOURCE VBP_CASC net8 GNDA GND sky130_fd_pr__nfet_01v8 L=2 W=0.5 nf=1 ad='int((1 + 1)/2) * 0.5 / 1 * 0.29'
+ as='int((1 + 2)/2) * 0.5 / 1 * 0.29' pd='2*int((1 + 1)/2) * (0.5 / 1 + 0.29)' ps='2*int((1 + 2)/2) * (0.5 / 1 + 0.29)'
+ nrd='0.29 / 0.5 ' nrs='0.29 / 0.5 ' sa=0 sb=0 sd=0 mult=1 m=1
XMP_CASC_BIAS1 net11 VBP_CASC VDD VDD sky130_fd_pr__pfet_01v8 L=0.5 W=0.5 nf=1 ad='int((1 + 1)/2) * 0.5 / 1 * 0.29'
+ as='int((1 + 2)/2) * 0.5 / 1 * 0.29' pd='2*int((1 + 1)/2) * (0.5 / 1 + 0.29)' ps='2*int((1 + 2)/2) * (0.5 / 1 + 0.29)'
+ nrd='0.29 / 0.5 ' nrs='0.29 / 0.5 ' sa=0 sb=0 sd=0 mult=1 m=1
XMN_CASC_BIAS7 net17 VBN_CASC net16 GND sky130_fd_pr__nfet_01v8 L=0.5 W=0.5 nf=1 ad='int((1 + 1)/2) * 0.5 / 1 * 0.29'
+ as='int((1 + 2)/2) * 0.5 / 1 * 0.29' pd='2*int((1 + 1)/2) * (0.5 / 1 + 0.29)' ps='2*int((1 + 2)/2) * (0.5 / 1 + 0.29)'
+ nrd='0.29 / 0.5 ' nrs='0.29 / 0.5 ' sa=0 sb=0 sd=0 mult=1 m=1
XMN_CASC_BIAS6 net18 VBN_CASC net17 GND sky130_fd_pr__nfet_01v8 L=0.5 W=0.5 nf=1 ad='int((1 + 1)/2) * 0.5 / 1 * 0.29'
+ as='int((1 + 2)/2) * 0.5 / 1 * 0.29' pd='2*int((1 + 1)/2) * (0.5 / 1 + 0.29)' ps='2*int((1 + 2)/2) * (0.5 / 1 + 0.29)'
+ nrd='0.29 / 0.5 ' nrs='0.29 / 0.5 ' sa=0 sb=0 sd=0 mult=1 m=1
XMP_CASC_BIAS2 net10 VBP_CASC net11 VDD sky130_fd_pr__pfet_01v8 L=0.5 W=0.5 nf=1 ad='int((1 + 1)/2) * 0.5 / 1 * 0.29'
+ as='int((1 + 2)/2) * 0.5 / 1 * 0.29' pd='2*int((1 + 1)/2) * (0.5 / 1 + 0.29)' ps='2*int((1 + 2)/2) * (0.5 / 1 + 0.29)'
+ nrd='0.29 / 0.5 ' nrs='0.29 / 0.5 ' sa=0 sb=0 sd=0 mult=1 m=1
XMP_CASC_BIAS3 VBP_CASC VBP_CASC net10 VDD sky130_fd_pr__pfet_01v8 L=0.5 W=0.5 nf=1 ad='int((1 + 1)/2) * 0.5 / 1 * 0.29'
+ as='int((1 + 2)/2) * 0.5 / 1 * 0.29' pd='2*int((1 + 1)/2) * (0.5 / 1 + 0.29)' ps='2*int((1 + 2)/2) * (0.5 / 1 + 0.29)'
+ nrd='0.29 / 0.5 ' nrs='0.29 / 0.5 ' sa=0 sb=0 sd=0 mult=1 m=1
XMN_CASC_BIAS5 net19 VBN_CASC net18 GND sky130_fd_pr__nfet_01v8 L=0.5 W=0.5 nf=1 ad='int((1 + 1)/2) * 0.5 / 1 * 0.29'
+ as='int((1 + 2)/2) * 0.5 / 1 * 0.29' pd='2*int((1 + 1)/2) * (0.5 / 1 + 0.29)' ps='2*int((1 + 2)/2) * (0.5 / 1 + 0.29)'
+ nrd='0.29 / 0.5 ' nrs='0.29 / 0.5 ' sa=0 sb=0 sd=0 mult=1 m=1
XMN_CASC_BIAS4 net20 VBN_CASC net19 GND sky130_fd_pr__nfet_01v8 L=0.5 W=0.5 nf=1 ad='int((1 + 1)/2) * 0.5 / 1 * 0.29'
+ as='int((1 + 2)/2) * 0.5 / 1 * 0.29' pd='2*int((1 + 1)/2) * (0.5 / 1 + 0.29)' ps='2*int((1 + 2)/2) * (0.5 / 1 + 0.29)'
+ nrd='0.29 / 0.5 ' nrs='0.29 / 0.5 ' sa=0 sb=0 sd=0 mult=1 m=1
XMN_CASC_BIAS3 net21 VBN_CASC net20 GND sky130_fd_pr__nfet_01v8 L=0.5 W=0.5 nf=1 ad='int((1 + 1)/2) * 0.5 / 1 * 0.29'
+ as='int((1 + 2)/2) * 0.5 / 1 * 0.29' pd='2*int((1 + 1)/2) * (0.5 / 1 + 0.29)' ps='2*int((1 + 2)/2) * (0.5 / 1 + 0.29)'
+ nrd='0.29 / 0.5 ' nrs='0.29 / 0.5 ' sa=0 sb=0 sd=0 mult=1 m=1
XMN_CASC_BIAS1 VBN_CASC VBN_CASC net22 GND sky130_fd_pr__nfet_01v8 L=0.5 W=0.5 nf=1 ad='int((1 + 1)/2) * 0.5 / 1 * 0.29'
+ as='int((1 + 2)/2) * 0.5 / 1 * 0.29' pd='2*int((1 + 1)/2) * (0.5 / 1 + 0.29)' ps='2*int((1 + 2)/2) * (0.5 / 1 + 0.29)'
+ nrd='0.29 / 0.5 ' nrs='0.29 / 0.5 ' sa=0 sb=0 sd=0 mult=1 m=1
XMN_CASC_BIAS2 net22 VBN_CASC net21 GND sky130_fd_pr__nfet_01v8 L=0.5 W=0.5 nf=1 ad='int((1 + 1)/2) * 0.5 / 1 * 0.29'
+ as='int((1 + 2)/2) * 0.5 / 1 * 0.29' pd='2*int((1 + 1)/2) * (0.5 / 1 + 0.29)' ps='2*int((1 + 2)/2) * (0.5 / 1 + 0.29)'
+ nrd='0.29 / 0.5 ' nrs='0.29 / 0.5 ' sa=0 sb=0 sd=0 mult=1 m=1
XMN_SW1 net8 EN_B GNDA GND sky130_fd_pr__nfet_01v8 L=1 W=1 nf=1 ad='int((1 + 1)/2) * 1 / 1 * 0.29' as='int((1 + 2)/2) * 1 / 1 * 0.29'
+ pd='2*int((1 + 1)/2) * (1 / 1 + 0.29)' ps='2*int((1 + 2)/2) * (1 / 1 + 0.29)' nrd='0.29 / 1 ' nrs='0.29 / 1 '
+ sa=0 sb=0 sd=0 mult=1 m=1
XMP_SW1 net9 EN VDD VDD sky130_fd_pr__pfet_01v8 L=2 W=2 nf=1 ad='int((1 + 1)/2) * 2 / 1 * 0.29' as='int((1 + 2)/2) * 2 / 1 * 0.29'
+ pd='2*int((1 + 1)/2) * (2 / 1 + 0.29)' ps='2*int((1 + 2)/2) * (2 / 1 + 0.29)' nrd='0.29 / 2 ' nrs='0.29 / 2 '
+ sa=0 sb=0 sd=0 mult=1 m=1
XMP_SW2 VBP_CASC EN VDD VDD sky130_fd_pr__pfet_01v8 L=2 W=2 nf=1 ad='int((1 + 1)/2) * 2 / 1 * 0.29' as='int((1 + 2)/2) * 2 / 1 * 0.29'
+ pd='2*int((1 + 1)/2) * (2 / 1 + 0.29)' ps='2*int((1 + 2)/2) * (2 / 1 + 0.29)' nrd='0.29 / 2 ' nrs='0.29 / 2 '
+ sa=0 sb=0 sd=0 mult=1 m=1
XMN_SW2 VBN_CASC EN_B GNDA GND sky130_fd_pr__nfet_01v8 L=2 W=1 nf=1 ad='int((1 + 1)/2) * 1 / 1 * 0.29'
+ as='int((1 + 2)/2) * 1 / 1 * 0.29' pd='2*int((1 + 1)/2) * (1 / 1 + 0.29)' ps='2*int((1 + 2)/2) * (1 / 1 + 0.29)'
+ nrd='0.29 / 1 ' nrs='0.29 / 1 ' sa=0 sb=0 sd=0 mult=1 m=1
XMP_SW3 net5 EN VDD VDD sky130_fd_pr__pfet_01v8 L=2 W=2 nf=1 ad='int((1 + 1)/2) * 2 / 1 * 0.29' as='int((1 + 2)/2) * 2 / 1 * 0.29'
+ pd='2*int((1 + 1)/2) * (2 / 1 + 0.29)' ps='2*int((1 + 2)/2) * (2 / 1 + 0.29)' nrd='0.29 / 2 ' nrs='0.29 / 2 '
+ sa=0 sb=0 sd=0 mult=1 m=1
.save v(vdd)
.save v(net7)
XM1 VBP_TOP MN_TAIL_BIAS net12 GND sky130_fd_pr__nfet_01v8 L=4 W=10 nf=1 ad='int((1 + 1)/2) * 10 / 1 * 0.29'
+ as='int((1 + 2)/2) * 10 / 1 * 0.29' pd='2*int((1 + 1)/2) * (10 / 1 + 0.29)' ps='2*int((1 + 2)/2) * (10 / 1 + 0.29)'
+ nrd='0.29 / 10 ' nrs='0.29 / 10 ' sa=0 sb=0 sd=0 mult=16 m=16
XM3 VBP_TOP VBP_TOP VDD VDD sky130_fd_pr__pfet_01v8 L=2 W=2 nf=1 ad='int((1 + 1)/2) * 2 / 1 * 0.29' as='int((1 + 2)/2) * 2 / 1 * 0.29'
+ pd='2*int((1 + 1)/2) * (2 / 1 + 0.29)' ps='2*int((1 + 2)/2) * (2 / 1 + 0.29)' nrd='0.29 / 2 ' nrs='0.29 / 2 '
+ sa=0 sb=0 sd=0 mult=1 m=1
XM4 MN_TAIL_BIAS VBP_TOP VDD VDD sky130_fd_pr__pfet_01v8 L=2 W=2 nf=1 ad='int((1 + 1)/2) * 2 / 1 * 0.29'
+ as='int((1 + 2)/2) * 2 / 1 * 0.29' pd='2*int((1 + 1)/2) * (2 / 1 + 0.29)' ps='2*int((1 + 2)/2) * (2 / 1 + 0.29)'
+ nrd='0.29 / 2 ' nrs='0.29 / 2 ' sa=0 sb=0 sd=0 mult=1 m=1
XM10 MN_TAIL_BIAS MN_TAIL_BIAS GNDA GND sky130_fd_pr__nfet_01v8 L=4 W=10 nf=1 ad='int((1 + 1)/2) * 10 / 1 * 0.29'
+ as='int((1 + 2)/2) * 10 / 1 * 0.29' pd='2*int((1 + 1)/2) * (10 / 1 + 0.29)' ps='2*int((1 + 2)/2) * (10 / 1 + 0.29)'
+ nrd='0.29 / 10 ' nrs='0.29 / 10 ' sa=0 sb=0 sd=0 mult=4 m=4
XM16 MN_TAIL_BIAS EN_B GNDA GND sky130_fd_pr__nfet_01v8 L=6.4 W=0.5 nf=1 ad='int((1 + 1)/2) * 0.5 / 1 * 0.29'
+ as='int((1 + 2)/2) * 0.5 / 1 * 0.29' pd='2*int((1 + 1)/2) * (0.5 / 1 + 0.29)' ps='2*int((1 + 2)/2) * (0.5 / 1 + 0.29)'
+ nrd='0.29 / 0.5 ' nrs='0.29 / 0.5 ' sa=0 sb=0 sd=0 mult=1 m=1
XR14 net23 net12 GNDA sky130_fd_pr__res_xhigh_po_1p41 L=6.4 mult=1 m=1
XR15 net24 net23 GNDA sky130_fd_pr__res_xhigh_po_1p41 L=6.4 mult=1 m=1
XR16 net25 net24 GNDA sky130_fd_pr__res_xhigh_po_1p41 L=6.4 mult=1 m=1
XR17 net26 net25 GNDA sky130_fd_pr__res_xhigh_po_1p41 L=6.4 mult=1 m=1
XR18 net27 net26 GNDA sky130_fd_pr__res_xhigh_po_1p41 L=6.4 mult=1 m=1
XR19 net28 net27 GNDA sky130_fd_pr__res_xhigh_po_1p41 L=6.4 mult=1 m=1
XR20 net29 net28 GNDA sky130_fd_pr__res_xhigh_po_1p41 L=6.4 mult=1 m=1
XR21 net30 net29 GNDA sky130_fd_pr__res_xhigh_po_1p41 L=6.4 mult=1 m=1
XR22 GNDA net30 GNDA sky130_fd_pr__res_xhigh_po_1p41 L=6.4 mult=1 m=1
XM15 VBP_TOP EN VDD VDD sky130_fd_pr__pfet_01v8 L=1 W=0.5 nf=1 ad='int((1 + 1)/2) * 0.5 / 1 * 0.29' as='int((1 + 2)/2) * 0.5 / 1 * 0.29'
+ pd='2*int((1 + 1)/2) * (0.5 / 1 + 0.29)' ps='2*int((1 + 2)/2) * (0.5 / 1 + 0.29)' nrd='0.29 / 0.5 ' nrs='0.29 / 0.5 '
+ sa=0 sb=0 sd=0 mult=1 m=1
XM2 VSTRP_IP VBP_TOP VDD VDD sky130_fd_pr__pfet_01v8 L=2 W=2 nf=1 ad='int((1 + 1)/2) * 2 / 1 * 0.29'
+ as='int((1 + 2)/2) * 2 / 1 * 0.29' pd='2*int((1 + 1)/2) * (2 / 1 + 0.29)' ps='2*int((1 + 2)/2) * (2 / 1 + 0.29)'
+ nrd='0.29 / 2 ' nrs='0.29 / 2 ' sa=0 sb=0 sd=0 mult=7 m=7
XM19 VSTRP_IP VDD net31 GNDA sky130_fd_pr__nfet_01v8 L=10 W=0.5 nf=1 ad='int((1 + 1)/2) * 0.5 / 1 * 0.29'
+ as='int((1 + 2)/2) * 0.5 / 1 * 0.29' pd='2*int((1 + 1)/2) * (0.5 / 1 + 0.29)' ps='2*int((1 + 2)/2) * (0.5 / 1 + 0.29)'
+ nrd='0.29 / 0.5 ' nrs='0.29 / 0.5 ' sa=0 sb=0 sd=0 mult=1 m=1
XM20 net31 VDD net32 GNDA sky130_fd_pr__nfet_01v8 L=10 W=0.5 nf=1 ad='int((1 + 1)/2) * 0.5 / 1 * 0.29'
+ as='int((1 + 2)/2) * 0.5 / 1 * 0.29' pd='2*int((1 + 1)/2) * (0.5 / 1 + 0.29)' ps='2*int((1 + 2)/2) * (0.5 / 1 + 0.29)'
+ nrd='0.29 / 0.5 ' nrs='0.29 / 0.5 ' sa=0 sb=0 sd=0 mult=1 m=1
XM21 net32 VDD net33 GNDA sky130_fd_pr__nfet_01v8 L=10 W=0.5 nf=1 ad='int((1 + 1)/2) * 0.5 / 1 * 0.29'
+ as='int((1 + 2)/2) * 0.5 / 1 * 0.29' pd='2*int((1 + 1)/2) * (0.5 / 1 + 0.29)' ps='2*int((1 + 2)/2) * (0.5 / 1 + 0.29)'
+ nrd='0.29 / 0.5 ' nrs='0.29 / 0.5 ' sa=0 sb=0 sd=0 mult=1 m=1
XM26 net33 VDD net34 GNDA sky130_fd_pr__nfet_01v8 L=10 W=0.5 nf=1 ad='int((1 + 1)/2) * 0.5 / 1 * 0.29'
+ as='int((1 + 2)/2) * 0.5 / 1 * 0.29' pd='2*int((1 + 1)/2) * (0.5 / 1 + 0.29)' ps='2*int((1 + 2)/2) * (0.5 / 1 + 0.29)'
+ nrd='0.29 / 0.5 ' nrs='0.29 / 0.5 ' sa=0 sb=0 sd=0 mult=1 m=1
XM27 net34 VDD net35 GNDA sky130_fd_pr__nfet_01v8 L=10 W=0.5 nf=1 ad='int((1 + 1)/2) * 0.5 / 1 * 0.29'
+ as='int((1 + 2)/2) * 0.5 / 1 * 0.29' pd='2*int((1 + 1)/2) * (0.5 / 1 + 0.29)' ps='2*int((1 + 2)/2) * (0.5 / 1 + 0.29)'
+ nrd='0.29 / 0.5 ' nrs='0.29 / 0.5 ' sa=0 sb=0 sd=0 mult=1 m=1
XM28 net35 VDD net36 GNDA sky130_fd_pr__nfet_01v8 L=10 W=0.5 nf=1 ad='int((1 + 1)/2) * 0.5 / 1 * 0.29'
+ as='int((1 + 2)/2) * 0.5 / 1 * 0.29' pd='2*int((1 + 1)/2) * (0.5 / 1 + 0.29)' ps='2*int((1 + 2)/2) * (0.5 / 1 + 0.29)'
+ nrd='0.29 / 0.5 ' nrs='0.29 / 0.5 ' sa=0 sb=0 sd=0 mult=1 m=1
XM29 net36 VDD net37 GNDA sky130_fd_pr__nfet_01v8 L=10 W=0.5 nf=1 ad='int((1 + 1)/2) * 0.5 / 1 * 0.29'
+ as='int((1 + 2)/2) * 0.5 / 1 * 0.29' pd='2*int((1 + 1)/2) * (0.5 / 1 + 0.29)' ps='2*int((1 + 2)/2) * (0.5 / 1 + 0.29)'
+ nrd='0.29 / 0.5 ' nrs='0.29 / 0.5 ' sa=0 sb=0 sd=0 mult=1 m=1
XM30 net37 VDD net38 GNDA sky130_fd_pr__nfet_01v8 L=10 W=0.5 nf=1 ad='int((1 + 1)/2) * 0.5 / 1 * 0.29'
+ as='int((1 + 2)/2) * 0.5 / 1 * 0.29' pd='2*int((1 + 1)/2) * (0.5 / 1 + 0.29)' ps='2*int((1 + 2)/2) * (0.5 / 1 + 0.29)'
+ nrd='0.29 / 0.5 ' nrs='0.29 / 0.5 ' sa=0 sb=0 sd=0 mult=1 m=1
XM31 net38 VDD net39 GNDA sky130_fd_pr__nfet_01v8 L=10 W=0.5 nf=1 ad='int((1 + 1)/2) * 0.5 / 1 * 0.29'
+ as='int((1 + 2)/2) * 0.5 / 1 * 0.29' pd='2*int((1 + 1)/2) * (0.5 / 1 + 0.29)' ps='2*int((1 + 2)/2) * (0.5 / 1 + 0.29)'
+ nrd='0.29 / 0.5 ' nrs='0.29 / 0.5 ' sa=0 sb=0 sd=0 mult=1 m=1
XM32 net39 VDD GNDA GNDA sky130_fd_pr__nfet_01v8 L=10 W=0.5 nf=1 ad='int((1 + 1)/2) * 0.5 / 1 * 0.29'
+ as='int((1 + 2)/2) * 0.5 / 1 * 0.29' pd='2*int((1 + 1)/2) * (0.5 / 1 + 0.29)' ps='2*int((1 + 2)/2) * (0.5 / 1 + 0.29)'
+ nrd='0.29 / 0.5 ' nrs='0.29 / 0.5 ' sa=0 sb=0 sd=0 mult=1 m=1
XM12 MN_TAIL_BIAS VSTRP_OUT net15 VDD sky130_fd_pr__pfet_01v8 L=4 W=0.5 nf=1 ad='int((1 + 1)/2) * 0.5 / 1 * 0.29'
+ as='int((1 + 2)/2) * 0.5 / 1 * 0.29' pd='2*int((1 + 1)/2) * (0.5 / 1 + 0.29)' ps='2*int((1 + 2)/2) * (0.5 / 1 + 0.29)'
+ nrd='0.29 / 0.5 ' nrs='0.29 / 0.5 ' sa=0 sb=0 sd=0 mult=1 m=1
XR24 net40 VDD GNDA sky130_fd_pr__res_xhigh_po_1p41 L=7.05 mult=1 m=1
XR25 net41 net40 GNDA sky130_fd_pr__res_xhigh_po_1p41 L=7.05 mult=1 m=1
XR26 net42 net41 GNDA sky130_fd_pr__res_xhigh_po_1p41 L=7.05 mult=1 m=1
XR27 net43 net42 GNDA sky130_fd_pr__res_xhigh_po_1p41 L=7.05 mult=1 m=1
XR28 net44 net43 GNDA sky130_fd_pr__res_xhigh_po_1p41 L=7.05 mult=1 m=1
XR29 net45 net44 GNDA sky130_fd_pr__res_xhigh_po_1p41 L=7.05 mult=1 m=1
XR30 net46 net45 GNDA sky130_fd_pr__res_xhigh_po_1p41 L=7.05 mult=1 m=1
XR31 net47 net46 GNDA sky130_fd_pr__res_xhigh_po_1p41 L=7.05 mult=1 m=1
XR34 net15 net47 GNDA sky130_fd_pr__res_xhigh_po_1p41 L=7.05 mult=1 m=1
XM5 EN_B EN GNDA GND sky130_fd_pr__nfet_01v8 L=0.15 W=1 nf=1 ad='int((1 + 1)/2) * 1 / 1 * 0.29' as='int((1 + 2)/2) * 1 / 1 * 0.29'
+ pd='2*int((1 + 1)/2) * (1 / 1 + 0.29)' ps='2*int((1 + 2)/2) * (1 / 1 + 0.29)' nrd='0.29 / 1 ' nrs='0.29 / 1 '
+ sa=0 sb=0 sd=0 mult=1 m=1
XM6 EN_B EN VDD VDD sky130_fd_pr__pfet_01v8 L=0.15 W=1 nf=1 ad='int((1 + 1)/2) * 1 / 1 * 0.29' as='int((1 + 2)/2) * 1 / 1 * 0.29'
+ pd='2*int((1 + 1)/2) * (1 / 1 + 0.29)' ps='2*int((1 + 2)/2) * (1 / 1 + 0.29)' nrd='0.29 / 1 ' nrs='0.29 / 1 '
+ sa=0 sb=0 sd=0 mult=1 m=1
XM38 VSTRP_OUT net14 net13 GND sky130_fd_pr__nfet_01v8 L=0.15 W=1 nf=1 ad='int((1 + 1)/2) * 1 / 1 * 0.29'
+ as='int((1 + 2)/2) * 1 / 1 * 0.29' pd='2*int((1 + 1)/2) * (1 / 1 + 0.29)' ps='2*int((1 + 2)/2) * (1 / 1 + 0.29)'
+ nrd='0.29 / 1 ' nrs='0.29 / 1 ' sa=0 sb=0 sd=0 mult=1 m=1
XM39 net13 EN GNDA GND sky130_fd_pr__nfet_01v8 L=0.15 W=1 nf=1 ad='int((1 + 1)/2) * 1 / 1 * 0.29' as='int((1 + 2)/2) * 1 / 1 * 0.29'
+ pd='2*int((1 + 1)/2) * (1 / 1 + 0.29)' ps='2*int((1 + 2)/2) * (1 / 1 + 0.29)' nrd='0.29 / 1 ' nrs='0.29 / 1 '
+ sa=0 sb=0 sd=0 mult=1 m=1
XM42 net14 VSTRP_IP GNDA GND sky130_fd_pr__nfet_01v8 L=0.15 W=1 nf=1 ad='int((1 + 1)/2) * 1 / 1 * 0.29'
+ as='int((1 + 2)/2) * 1 / 1 * 0.29' pd='2*int((1 + 1)/2) * (1 / 1 + 0.29)' ps='2*int((1 + 2)/2) * (1 / 1 + 0.29)'
+ nrd='0.29 / 1 ' nrs='0.29 / 1 ' sa=0 sb=0 sd=0 mult=1 m=1
XM43 net14 VSTRP_IP VDD VDD sky130_fd_pr__pfet_01v8 L=0.15 W=1 nf=1 ad='int((1 + 1)/2) * 1 / 1 * 0.29'
+ as='int((1 + 2)/2) * 1 / 1 * 0.29' pd='2*int((1 + 1)/2) * (1 / 1 + 0.29)' ps='2*int((1 + 2)/2) * (1 / 1 + 0.29)'
+ nrd='0.29 / 1 ' nrs='0.29 / 1 ' sa=0 sb=0 sd=0 mult=1 m=1
XM13 VSTRP_OUT net14 VDD VDD sky130_fd_pr__pfet_01v8 L=0.15 W=1 nf=1 ad='int((1 + 1)/2) * 1 / 1 * 0.29'
+ as='int((1 + 2)/2) * 1 / 1 * 0.29' pd='2*int((1 + 1)/2) * (1 / 1 + 0.29)' ps='2*int((1 + 2)/2) * (1 / 1 + 0.29)'
+ nrd='0.29 / 1 ' nrs='0.29 / 1 ' sa=0 sb=0 sd=0 mult=1 m=1
XM14 VSTRP_OUT EN_B VDD VDD sky130_fd_pr__pfet_01v8 L=0.15 W=1 nf=1 ad='int((1 + 1)/2) * 1 / 1 * 0.29'
+ as='int((1 + 2)/2) * 1 / 1 * 0.29' pd='2*int((1 + 1)/2) * (1 / 1 + 0.29)' ps='2*int((1 + 2)/2) * (1 / 1 + 0.29)'
+ nrd='0.29 / 1 ' nrs='0.29 / 1 ' sa=0 sb=0 sd=0 mult=1 m=1
XM9 net8 VBP_TOP VDD VDD sky130_fd_pr__pfet_01v8 L=2 W=2 nf=1 ad='int((1 + 1)/2) * 2 / 1 * 0.29' as='int((1 + 2)/2) * 2 / 1 * 0.29'
+ pd='2*int((1 + 1)/2) * (2 / 1 + 0.29)' ps='2*int((1 + 2)/2) * (2 / 1 + 0.29)' nrd='0.29 / 2 ' nrs='0.29 / 2 '
+ sa=0 sb=0 sd=0 mult=2 m=2
.ends

.GLOBAL VDD
.end
